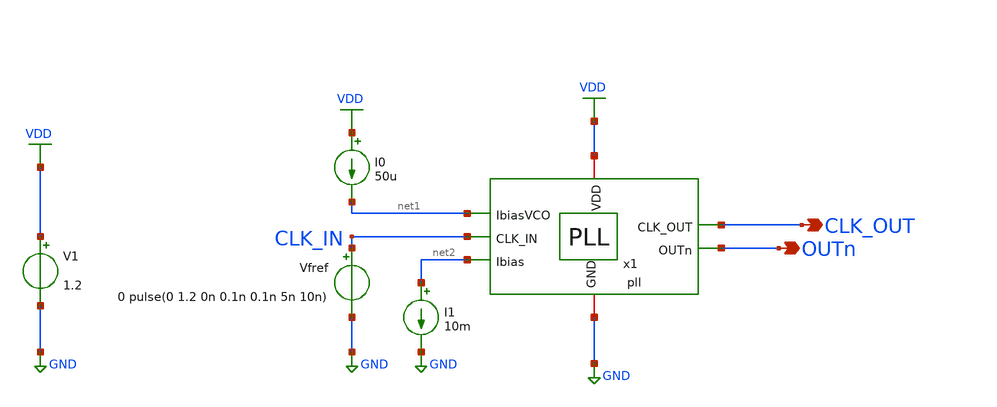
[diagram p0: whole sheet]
** sch_path: schematic/blocks/top-pll/top_pll_tb.sch
**.subckt top_pll_tb OUTn CLK_OUT
*.opin OUTn
*.opin CLK_OUT
V1 VDD GND 1.2
I0 VDD net1 50u
Vfref CLK_IN GND 0 pulse(0 1.2 0n 0.1n 0.1n 5n 10n)
I1 net2 GND 10m
x1 CLK_OUT CLK_IN net1 OUTn net2 VDD GND pll
**** begin user architecture code



*****************************************************
* PLL + DSM Frequency Divider Testbench (Optimized)
*****************************************************

.option temp=27
.param VDD=1.2

* ==============================
* Include Models & Stimuli
* ==============================
.include ./IHP_4nH_Inductor.spice
.include stimuli_test.cir

* ==============================
* Simulation Options (Optimized for Speed & Stability)
* ==============================
* gear method improves stability for long oscillator runs
* reltol=1e-3 prevents the simulator from bogging down on microscopic errors
.options reltol=1e-3 abstol=1e-9 vntol=1e-6 method=gear

* ==============================
* Initial Conditions (Speed Hack)
* ==============================
* Uncomment the line below to pre-charge the loop filter to your expected
* V_tune voltage (e.g., 0.6V). This skips the massive initial frequency jump.
* .ic v(x2.vctrl)=0.6

.control
  save all
  *save v(sdata) v(sclk) v(rst) v(en) v(UP) v(DN) v(VCTRL) v(CLK_IN) v(DSM_OUT) v(CLK_OUT)
  * Simulation accuracy options
  .options maxstep=10p reltol=1e-4 abstol=1e-9

 * Run long enough for PLL lock
  tran 20p 5u uic
  remzerovec
  write pll_top.raw
.endc






.lib cornerMOSlv.lib mos_tt
.lib cornerHBT.lib hbt_typ
.lib cornerRES.lib res_typ
.lib cornerCAP.lib cap_typ_stat
.include /foss/pdks/ihp-sg13g2/libs.ref/sg13g2_stdcell/spice/sg13g2_stdcell.spice
.global VDD GND


.param CP_N_L = 0.5u
.param CP_N_W = 10u
.param CP_P_M = 1
.param CP_P_L = 0.5u
.param CP_P_W = 30u
.param CP_N_M = 1
.param C_CP = 400p



**** end user architecture code
**.ends
.GLOBAL GND
.GLOBAL VDD
.end
